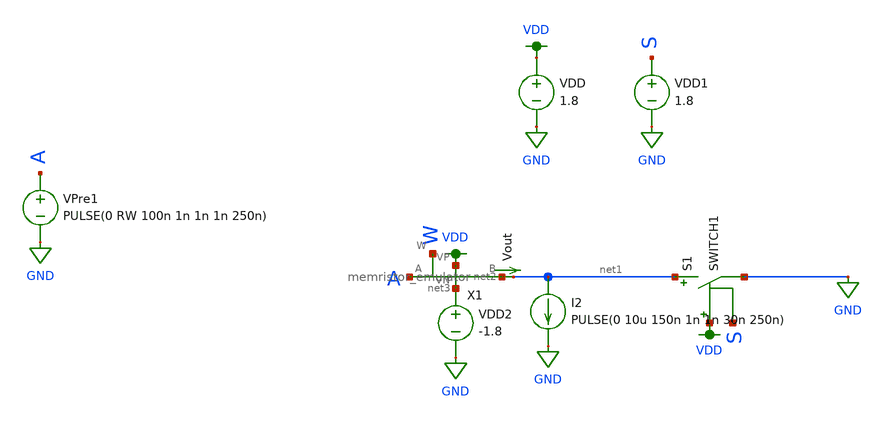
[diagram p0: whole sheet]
** sch_path: schematic/STDP_test.sch
**.subckt STDP_test
VDD VDD GND 1.8
Vout net2 net1 0
.save i(vout)
VDD2 net3 GND -1.8
X1 VDD net3 net2 A W memristor_emulator
I2 net1 GND PULSE(0 10u 150n 1n 1n 30n 250n)
VPre1 A GND PULSE(0 RW 100n 1n 1n 1n 250n)
S1 net1 GND VDD S SWITCH1
VDD1 S GND 1.8
**** begin user architecture code


.param RW = 1.8
.param C = 10u
.tran 0.1n 10u

.save all


.option wnflag=1
.param MC_SWITCH=0.0
.lib ~/skywater/skywater-pdk/libraries/sky130_fd_pr_ngspice/latest/models/sky130.lib.spice tt

**** end user architecture code
**.ends

* expanding   symbol:  /home/madvlsi/neuromorphic_computing_final/schematic/memristor_emulator.sym #
*+ of pins=5
** sym_path: schematic/memristor_emulator.sym
** sch_path: schematic/memristor_emulator.sch
.subckt memristor_emulator VP VN B A W
*.iopin VN
*.iopin VP
*.opin W
*.iopin B
*.iopin A
XM1 B W A B sky130_fd_pr__pfet_01v8 L=0.5 W=12 nf=1 ad='int((nf+1)/2) * W/nf * 0.29' as='int((nf+2)/2) * W/nf * 0.29'
+ pd='2*int((nf+1)/2) * (W/nf + 0.29)' ps='2*int((nf+2)/2) * (W/nf + 0.29)' nrd='0.29 / W' nrs='0.29 / W'
+ sa=0 sb=0 sd=0 mult=1 m=1
XM2 VP A W VP sky130_fd_pr__pfet_01v8 L=2 W=3 nf=1 ad='int((nf+1)/2) * W/nf * 0.29' as='int((nf+2)/2) * W/nf * 0.29'
+ pd='2*int((nf+1)/2) * (W/nf + 0.29)' ps='2*int((nf+2)/2) * (W/nf + 0.29)' nrd='0.29 / W' nrs='0.29 / W'
+ sa=0 sb=0 sd=0 mult=1 m=1
XM3 VN W VN VN sky130_fd_pr__nfet_01v8 L=20 W=20 nf=1 ad='int((nf+1)/2) * W/nf * 0.29' as='int((nf+2)/2) * W/nf * 0.29'
+ pd='2*int((nf+1)/2) * (W/nf + 0.29)' ps='2*int((nf+2)/2) * (W/nf + 0.29)' nrd='0.29 / W' nrs='0.29 / W'
+ sa=0 sb=0 sd=0 mult=1 m=1
XM4 VN B W VN sky130_fd_pr__nfet_01v8 L=3 W=2 nf=1 ad='int((nf+1)/2) * W/nf * 0.29' as='int((nf+2)/2) * W/nf * 0.29'
+ pd='2*int((nf+1)/2) * (W/nf + 0.29)' ps='2*int((nf+2)/2) * (W/nf + 0.29)' nrd='0.29 / W' nrs='0.29 / W'
+ sa=0 sb=0 sd=0 mult=1 m=1
.ends

.GLOBAL GND
.GLOBAL VDD
.end
